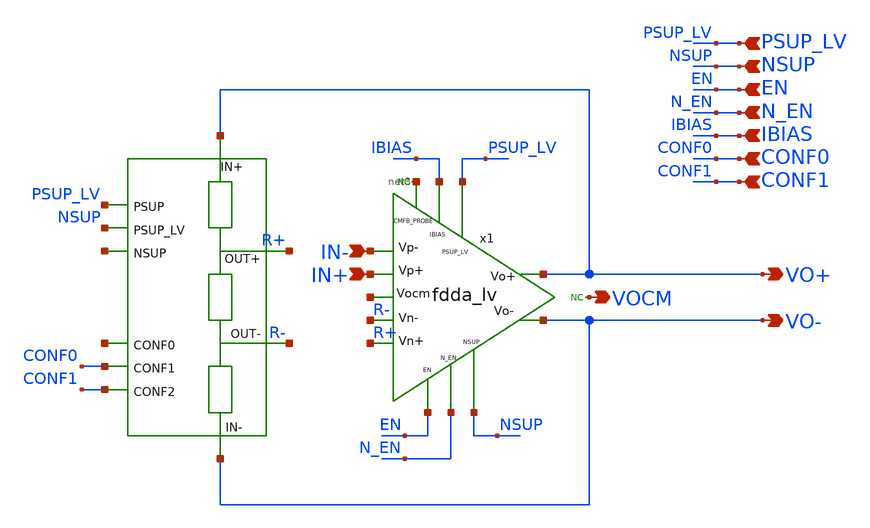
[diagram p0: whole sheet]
** sch_path: xschem/blocks/INA/INA.sch
**.subckt INA VO+ VO- IN+ IN- NSUP EN N_EN IBIAS PSUP_LV CONF0 CONF1 VOCM
*.opin VO+
*.opin VO-
*.ipin IN+
*.ipin IN-
*.ipin NSUP
*.ipin EN
*.ipin N_EN
*.ipin IBIAS
*.ipin PSUP_LV
*.ipin CONF0
*.ipin CONF1
*.opin VOCM
* noconn VOCM
* noconn #net3
x1 PSUP_LV IN- R- R+ IN+ VO+ VO- IBIAS N_EN EN NSUP net3 net4 fdda_lv
**.ends
.end
